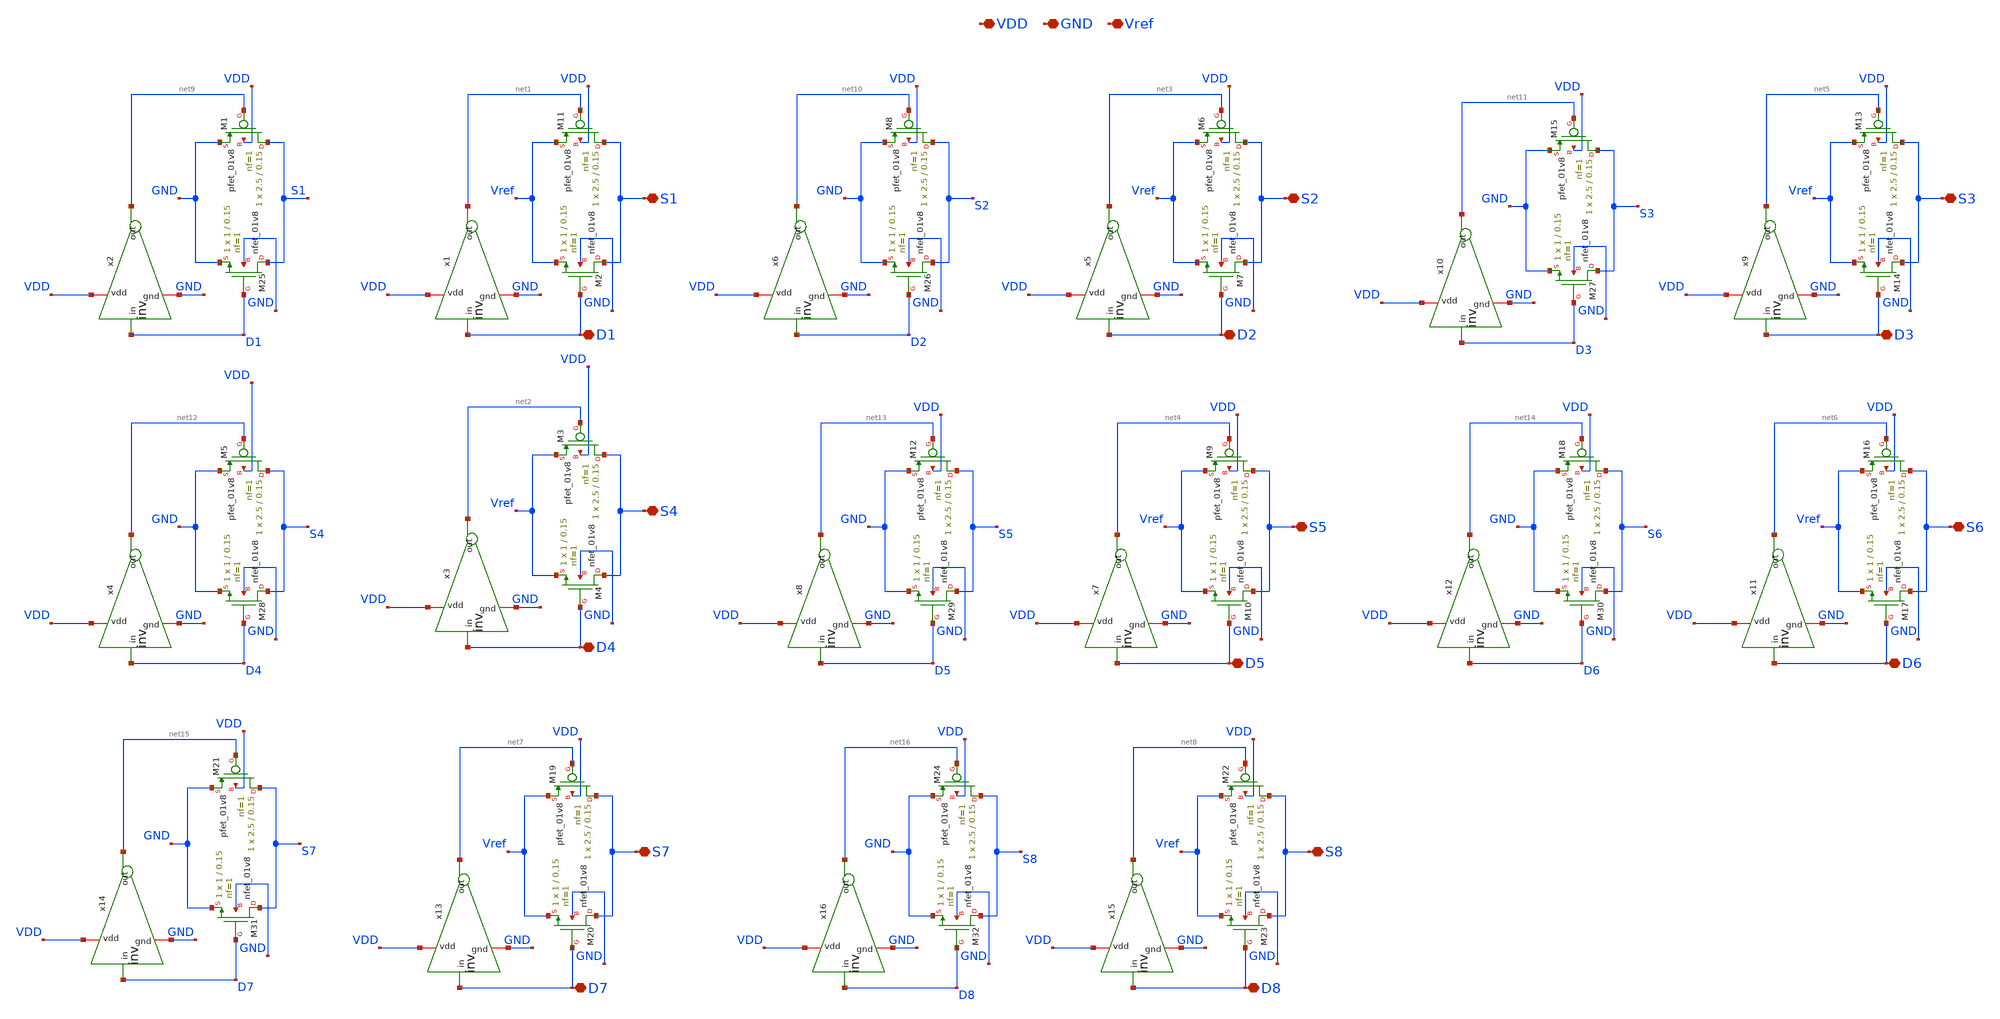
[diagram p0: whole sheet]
** sch_path: sar-adc/updated/Switch_Array.sch
**.subckt Switch_Array VDD GND D1 Vref S1 D4 S4 D2 S2 D5 S5 D3 S3 D6 S6 D7 S7 D8 S8
*.iopin VDD
*.iopin GND
*.iopin D1
*.iopin Vref
*.iopin S1
*.iopin D4
*.iopin S4
*.iopin D2
*.iopin S2
*.iopin D5
*.iopin S5
*.iopin D3
*.iopin S3
*.iopin D6
*.iopin S6
*.iopin D7
*.iopin S7
*.iopin D8
*.iopin S8
XM11 S1 net1 Vref VDD sky130_fd_pr__pfet_01v8 L=0.15 W=2.5 nf=1 ad='int((nf+1)/2) * W/nf * 0.29' as='int((nf+2)/2) * W/nf * 0.29'
+ pd='2*int((nf+1)/2) * (W/nf + 0.29)' ps='2*int((nf+2)/2) * (W/nf + 0.29)' nrd='0.29 / W' nrs='0.29 / W'
+ sa=0 sb=0 sd=0 mult=1 m=1
XM2 S1 D1 Vref GND sky130_fd_pr__nfet_01v8 L=0.15 W=1 nf=1 ad='int((1 + 1)/2) * 1 / 1 * 0.29' as='int((1 + 2)/2) * 1 / 1 * 0.29'
+ pd='2*int((1 + 1)/2) * (1 / 1 + 0.29)' ps='2*int((1 + 2)/2) * (1 / 1 + 0.29)' nrd='0.29 / 1 ' nrs='0.29 / 1 '
+ sa=0 sb=0 sd=0 mult=1 m=1
x1 VDD D1 net1 GND inv
XM3 S4 net2 Vref VDD sky130_fd_pr__pfet_01v8 L=0.15 W=2.5 nf=1 ad='int((nf+1)/2) * W/nf * 0.29' as='int((nf+2)/2) * W/nf * 0.29'
+ pd='2*int((nf+1)/2) * (W/nf + 0.29)' ps='2*int((nf+2)/2) * (W/nf + 0.29)' nrd='0.29 / W' nrs='0.29 / W'
+ sa=0 sb=0 sd=0 mult=1 m=1
XM4 S4 D4 Vref GND sky130_fd_pr__nfet_01v8 L=0.15 W=1 nf=1 ad='int((1 + 1)/2) * 1 / 1 * 0.29' as='int((1 + 2)/2) * 1 / 1 * 0.29'
+ pd='2*int((1 + 1)/2) * (1 / 1 + 0.29)' ps='2*int((1 + 2)/2) * (1 / 1 + 0.29)' nrd='0.29 / 1 ' nrs='0.29 / 1 '
+ sa=0 sb=0 sd=0 mult=1 m=1
x3 VDD D4 net2 GND inv
XM6 S2 net3 Vref VDD sky130_fd_pr__pfet_01v8 L=0.15 W=2.5 nf=1 ad='int((nf+1)/2) * W/nf * 0.29' as='int((nf+2)/2) * W/nf * 0.29'
+ pd='2*int((nf+1)/2) * (W/nf + 0.29)' ps='2*int((nf+2)/2) * (W/nf + 0.29)' nrd='0.29 / W' nrs='0.29 / W'
+ sa=0 sb=0 sd=0 mult=1 m=1
XM7 S2 D2 Vref GND sky130_fd_pr__nfet_01v8 L=0.15 W=1 nf=1 ad='int((1 + 1)/2) * 1 / 1 * 0.29' as='int((1 + 2)/2) * 1 / 1 * 0.29'
+ pd='2*int((1 + 1)/2) * (1 / 1 + 0.29)' ps='2*int((1 + 2)/2) * (1 / 1 + 0.29)' nrd='0.29 / 1 ' nrs='0.29 / 1 '
+ sa=0 sb=0 sd=0 mult=1 m=1
x5 VDD D2 net3 GND inv
XM9 S5 net4 Vref VDD sky130_fd_pr__pfet_01v8 L=0.15 W=2.5 nf=1 ad='int((nf+1)/2) * W/nf * 0.29' as='int((nf+2)/2) * W/nf * 0.29'
+ pd='2*int((nf+1)/2) * (W/nf + 0.29)' ps='2*int((nf+2)/2) * (W/nf + 0.29)' nrd='0.29 / W' nrs='0.29 / W'
+ sa=0 sb=0 sd=0 mult=1 m=1
XM10 S5 D5 Vref GND sky130_fd_pr__nfet_01v8 L=0.15 W=1 nf=1 ad='int((1 + 1)/2) * 1 / 1 * 0.29' as='int((1 + 2)/2) * 1 / 1 * 0.29'
+ pd='2*int((1 + 1)/2) * (1 / 1 + 0.29)' ps='2*int((1 + 2)/2) * (1 / 1 + 0.29)' nrd='0.29 / 1 ' nrs='0.29 / 1 '
+ sa=0 sb=0 sd=0 mult=1 m=1
x7 VDD D5 net4 GND inv
XM13 S3 net5 Vref VDD sky130_fd_pr__pfet_01v8 L=0.15 W=2.5 nf=1 ad='int((nf+1)/2) * W/nf * 0.29' as='int((nf+2)/2) * W/nf * 0.29'
+ pd='2*int((nf+1)/2) * (W/nf + 0.29)' ps='2*int((nf+2)/2) * (W/nf + 0.29)' nrd='0.29 / W' nrs='0.29 / W'
+ sa=0 sb=0 sd=0 mult=1 m=1
XM14 S3 D3 Vref GND sky130_fd_pr__nfet_01v8 L=0.15 W=1 nf=1 ad='int((1 + 1)/2) * 1 / 1 * 0.29' as='int((1 + 2)/2) * 1 / 1 * 0.29'
+ pd='2*int((1 + 1)/2) * (1 / 1 + 0.29)' ps='2*int((1 + 2)/2) * (1 / 1 + 0.29)' nrd='0.29 / 1 ' nrs='0.29 / 1 '
+ sa=0 sb=0 sd=0 mult=1 m=1
x9 VDD D3 net5 GND inv
XM16 S6 net6 Vref VDD sky130_fd_pr__pfet_01v8 L=0.15 W=2.5 nf=1 ad='int((nf+1)/2) * W/nf * 0.29' as='int((nf+2)/2) * W/nf * 0.29'
+ pd='2*int((nf+1)/2) * (W/nf + 0.29)' ps='2*int((nf+2)/2) * (W/nf + 0.29)' nrd='0.29 / W' nrs='0.29 / W'
+ sa=0 sb=0 sd=0 mult=1 m=1
XM17 S6 D6 Vref GND sky130_fd_pr__nfet_01v8 L=0.15 W=1 nf=1 ad='int((1 + 1)/2) * 1 / 1 * 0.29' as='int((1 + 2)/2) * 1 / 1 * 0.29'
+ pd='2*int((1 + 1)/2) * (1 / 1 + 0.29)' ps='2*int((1 + 2)/2) * (1 / 1 + 0.29)' nrd='0.29 / 1 ' nrs='0.29 / 1 '
+ sa=0 sb=0 sd=0 mult=1 m=1
x11 VDD D6 net6 GND inv
XM19 S7 net7 Vref VDD sky130_fd_pr__pfet_01v8 L=0.15 W=2.5 nf=1 ad='int((nf+1)/2) * W/nf * 0.29' as='int((nf+2)/2) * W/nf * 0.29'
+ pd='2*int((nf+1)/2) * (W/nf + 0.29)' ps='2*int((nf+2)/2) * (W/nf + 0.29)' nrd='0.29 / W' nrs='0.29 / W'
+ sa=0 sb=0 sd=0 mult=1 m=1
XM20 S7 D7 Vref GND sky130_fd_pr__nfet_01v8 L=0.15 W=1 nf=1 ad='int((1 + 1)/2) * 1 / 1 * 0.29' as='int((1 + 2)/2) * 1 / 1 * 0.29'
+ pd='2*int((1 + 1)/2) * (1 / 1 + 0.29)' ps='2*int((1 + 2)/2) * (1 / 1 + 0.29)' nrd='0.29 / 1 ' nrs='0.29 / 1 '
+ sa=0 sb=0 sd=0 mult=1 m=1
x13 VDD D7 net7 GND inv
XM22 S8 net8 Vref VDD sky130_fd_pr__pfet_01v8 L=0.15 W=2.5 nf=1 ad='int((nf+1)/2) * W/nf * 0.29' as='int((nf+2)/2) * W/nf * 0.29'
+ pd='2*int((nf+1)/2) * (W/nf + 0.29)' ps='2*int((nf+2)/2) * (W/nf + 0.29)' nrd='0.29 / W' nrs='0.29 / W'
+ sa=0 sb=0 sd=0 mult=1 m=1
XM23 S8 D8 Vref GND sky130_fd_pr__nfet_01v8 L=0.15 W=1 nf=1 ad='int((1 + 1)/2) * 1 / 1 * 0.29' as='int((1 + 2)/2) * 1 / 1 * 0.29'
+ pd='2*int((1 + 1)/2) * (1 / 1 + 0.29)' ps='2*int((1 + 2)/2) * (1 / 1 + 0.29)' nrd='0.29 / 1 ' nrs='0.29 / 1 '
+ sa=0 sb=0 sd=0 mult=1 m=1
x15 VDD D8 net8 GND inv
XM1 S1 net9 GND VDD sky130_fd_pr__pfet_01v8 L=0.15 W=2.5 nf=1 ad='int((nf+1)/2) * W/nf * 0.29' as='int((nf+2)/2) * W/nf * 0.29'
+ pd='2*int((nf+1)/2) * (W/nf + 0.29)' ps='2*int((nf+2)/2) * (W/nf + 0.29)' nrd='0.29 / W' nrs='0.29 / W'
+ sa=0 sb=0 sd=0 mult=1 m=1
XM25 S1 D1 GND GND sky130_fd_pr__nfet_01v8 L=0.15 W=1 nf=1 ad='int((1 + 1)/2) * 1 / 1 * 0.29' as='int((1 + 2)/2) * 1 / 1 * 0.29'
+ pd='2*int((1 + 1)/2) * (1 / 1 + 0.29)' ps='2*int((1 + 2)/2) * (1 / 1 + 0.29)' nrd='0.29 / 1 ' nrs='0.29 / 1 '
+ sa=0 sb=0 sd=0 mult=1 m=1
x2 VDD D1 net9 GND inv
XM8 S2 net10 GND VDD sky130_fd_pr__pfet_01v8 L=0.15 W=2.5 nf=1 ad='int((nf+1)/2) * W/nf * 0.29' as='int((nf+2)/2) * W/nf * 0.29'
+ pd='2*int((nf+1)/2) * (W/nf + 0.29)' ps='2*int((nf+2)/2) * (W/nf + 0.29)' nrd='0.29 / W' nrs='0.29 / W'
+ sa=0 sb=0 sd=0 mult=1 m=1
XM26 S2 D2 GND GND sky130_fd_pr__nfet_01v8 L=0.15 W=1 nf=1 ad='int((1 + 1)/2) * 1 / 1 * 0.29' as='int((1 + 2)/2) * 1 / 1 * 0.29'
+ pd='2*int((1 + 1)/2) * (1 / 1 + 0.29)' ps='2*int((1 + 2)/2) * (1 / 1 + 0.29)' nrd='0.29 / 1 ' nrs='0.29 / 1 '
+ sa=0 sb=0 sd=0 mult=1 m=1
x6 VDD D2 net10 GND inv
XM15 S3 net11 GND VDD sky130_fd_pr__pfet_01v8 L=0.15 W=2.5 nf=1 ad='int((nf+1)/2) * W/nf * 0.29' as='int((nf+2)/2) * W/nf * 0.29'
+ pd='2*int((nf+1)/2) * (W/nf + 0.29)' ps='2*int((nf+2)/2) * (W/nf + 0.29)' nrd='0.29 / W' nrs='0.29 / W'
+ sa=0 sb=0 sd=0 mult=1 m=1
XM27 S3 D3 GND GND sky130_fd_pr__nfet_01v8 L=0.15 W=1 nf=1 ad='int((1 + 1)/2) * 1 / 1 * 0.29' as='int((1 + 2)/2) * 1 / 1 * 0.29'
+ pd='2*int((1 + 1)/2) * (1 / 1 + 0.29)' ps='2*int((1 + 2)/2) * (1 / 1 + 0.29)' nrd='0.29 / 1 ' nrs='0.29 / 1 '
+ sa=0 sb=0 sd=0 mult=1 m=1
x10 VDD D3 net11 GND inv
XM5 S4 net12 GND VDD sky130_fd_pr__pfet_01v8 L=0.15 W=2.5 nf=1 ad='int((nf+1)/2) * W/nf * 0.29' as='int((nf+2)/2) * W/nf * 0.29'
+ pd='2*int((nf+1)/2) * (W/nf + 0.29)' ps='2*int((nf+2)/2) * (W/nf + 0.29)' nrd='0.29 / W' nrs='0.29 / W'
+ sa=0 sb=0 sd=0 mult=1 m=1
XM28 S4 D4 GND GND sky130_fd_pr__nfet_01v8 L=0.15 W=1 nf=1 ad='int((1 + 1)/2) * 1 / 1 * 0.29' as='int((1 + 2)/2) * 1 / 1 * 0.29'
+ pd='2*int((1 + 1)/2) * (1 / 1 + 0.29)' ps='2*int((1 + 2)/2) * (1 / 1 + 0.29)' nrd='0.29 / 1 ' nrs='0.29 / 1 '
+ sa=0 sb=0 sd=0 mult=1 m=1
x4 VDD D4 net12 GND inv
XM12 S5 net13 GND VDD sky130_fd_pr__pfet_01v8 L=0.15 W=2.5 nf=1 ad='int((nf+1)/2) * W/nf * 0.29' as='int((nf+2)/2) * W/nf * 0.29'
+ pd='2*int((nf+1)/2) * (W/nf + 0.29)' ps='2*int((nf+2)/2) * (W/nf + 0.29)' nrd='0.29 / W' nrs='0.29 / W'
+ sa=0 sb=0 sd=0 mult=1 m=1
XM29 S5 D5 GND GND sky130_fd_pr__nfet_01v8 L=0.15 W=1 nf=1 ad='int((1 + 1)/2) * 1 / 1 * 0.29' as='int((1 + 2)/2) * 1 / 1 * 0.29'
+ pd='2*int((1 + 1)/2) * (1 / 1 + 0.29)' ps='2*int((1 + 2)/2) * (1 / 1 + 0.29)' nrd='0.29 / 1 ' nrs='0.29 / 1 '
+ sa=0 sb=0 sd=0 mult=1 m=1
x8 VDD D5 net13 GND inv
XM18 S6 net14 GND VDD sky130_fd_pr__pfet_01v8 L=0.15 W=2.5 nf=1 ad='int((nf+1)/2) * W/nf * 0.29' as='int((nf+2)/2) * W/nf * 0.29'
+ pd='2*int((nf+1)/2) * (W/nf + 0.29)' ps='2*int((nf+2)/2) * (W/nf + 0.29)' nrd='0.29 / W' nrs='0.29 / W'
+ sa=0 sb=0 sd=0 mult=1 m=1
XM30 S6 D6 GND GND sky130_fd_pr__nfet_01v8 L=0.15 W=1 nf=1 ad='int((1 + 1)/2) * 1 / 1 * 0.29' as='int((1 + 2)/2) * 1 / 1 * 0.29'
+ pd='2*int((1 + 1)/2) * (1 / 1 + 0.29)' ps='2*int((1 + 2)/2) * (1 / 1 + 0.29)' nrd='0.29 / 1 ' nrs='0.29 / 1 '
+ sa=0 sb=0 sd=0 mult=1 m=1
x12 VDD D6 net14 GND inv
XM21 S7 net15 GND VDD sky130_fd_pr__pfet_01v8 L=0.15 W=2.5 nf=1 ad='int((nf+1)/2) * W/nf * 0.29' as='int((nf+2)/2) * W/nf * 0.29'
+ pd='2*int((nf+1)/2) * (W/nf + 0.29)' ps='2*int((nf+2)/2) * (W/nf + 0.29)' nrd='0.29 / W' nrs='0.29 / W'
+ sa=0 sb=0 sd=0 mult=1 m=1
XM31 S7 D7 GND GND sky130_fd_pr__nfet_01v8 L=0.15 W=1 nf=1 ad='int((1 + 1)/2) * 1 / 1 * 0.29' as='int((1 + 2)/2) * 1 / 1 * 0.29'
+ pd='2*int((1 + 1)/2) * (1 / 1 + 0.29)' ps='2*int((1 + 2)/2) * (1 / 1 + 0.29)' nrd='0.29 / 1 ' nrs='0.29 / 1 '
+ sa=0 sb=0 sd=0 mult=1 m=1
x14 VDD D7 net15 GND inv
XM24 S8 net16 GND VDD sky130_fd_pr__pfet_01v8 L=0.15 W=2.5 nf=1 ad='int((nf+1)/2) * W/nf * 0.29' as='int((nf+2)/2) * W/nf * 0.29'
+ pd='2*int((nf+1)/2) * (W/nf + 0.29)' ps='2*int((nf+2)/2) * (W/nf + 0.29)' nrd='0.29 / W' nrs='0.29 / W'
+ sa=0 sb=0 sd=0 mult=1 m=1
XM32 S8 D8 GND GND sky130_fd_pr__nfet_01v8 L=0.15 W=1 nf=1 ad='int((1 + 1)/2) * 1 / 1 * 0.29' as='int((1 + 2)/2) * 1 / 1 * 0.29'
+ pd='2*int((1 + 1)/2) * (1 / 1 + 0.29)' ps='2*int((1 + 2)/2) * (1 / 1 + 0.29)' nrd='0.29 / 1 ' nrs='0.29 / 1 '
+ sa=0 sb=0 sd=0 mult=1 m=1
x16 VDD D8 net16 GND inv
**.ends

* expanding   symbol:  inv.sym # of pins=4
** sym_path: sar-adc/updated/inv.sym
** sch_path: sar-adc/updated/inv.sch
.subckt inv vdd in out gnd
*.ipin in
*.opin out
*.iopin vdd
*.iopin gnd
XM2 out in gnd gnd sky130_fd_pr__nfet_01v8 L=0.15 W=1 nf=1 ad='int((1 + 1)/2) * 1 / 1 * 0.29' as='int((1 + 2)/2) * 1 / 1 * 0.29'
+ pd='2*int((1 + 1)/2) * (1 / 1 + 0.29)' ps='2*int((1 + 2)/2) * (1 / 1 + 0.29)' nrd='0.29 / 1 ' nrs='0.29 / 1 '
+ sa=0 sb=0 sd=0 mult=1 m=1
XM11 out in vdd vdd sky130_fd_pr__pfet_01v8 L=0.15 W=2.5 nf=1 ad='int((nf+1)/2) * W/nf * 0.29' as='int((nf+2)/2) * W/nf * 0.29'
+ pd='2*int((nf+1)/2) * (W/nf + 0.29)' ps='2*int((nf+2)/2) * (W/nf + 0.29)' nrd='0.29 / W' nrs='0.29 / W'
+ sa=0 sb=0 sd=0 mult=1 m=1
.ends

.end
